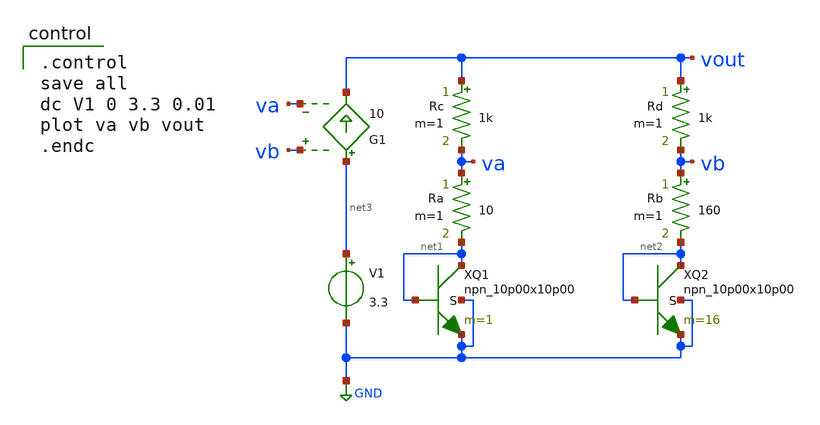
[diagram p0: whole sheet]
** sch_path: bgr/npn-diode-delta-4.sch
**.subckt npn-diode-delta-4
XQ1 net1 net1 GND GND npn_10p00x10p00 m=1
XQ2 net2 net2 GND GND npn_10p00x10p00 m=16
Rb vb net2 160 m=1
Ra va net1 10 m=1
Rc vout va 1k m=1
Rd vout vb 1k m=1
V1 net3 GND 3.3
G1 net3 vout vb va 10
**** begin user architecture code

.include $::180MCU_MODELS/design.ngspice
.lib $::180MCU_MODELS/sm141064.ngspice typical
.lib $::180MCU_MODELS/sm141064.ngspice res_typical
.lib $::180MCU_MODELS/sm141064.ngspice moscap_typical
.lib $::180MCU_MODELS/sm141064.ngspice bjt_typical
* .lib $::180MCU_MODELS/sm141064.ngspice res_statistical


.control
save all
dc V1 0 3.3 0.01
plot va vb vout
.endc

**** end user architecture code
**.ends
.GLOBAL GND
.end
